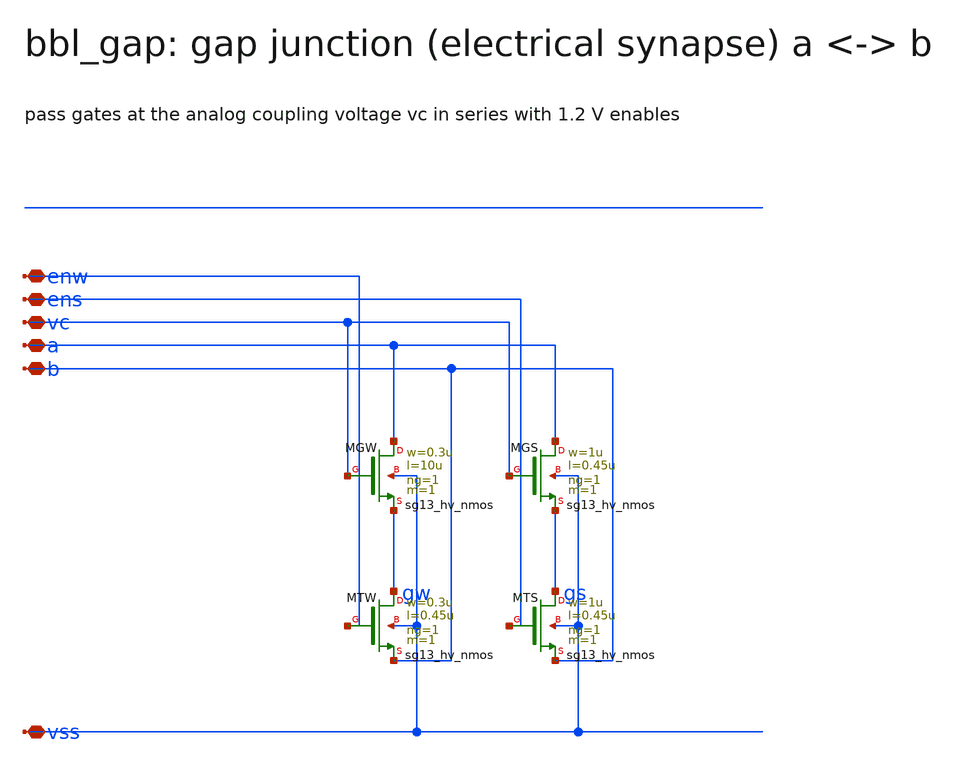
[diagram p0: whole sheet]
** sch_path: schematic/xschem/bbl_gap.sch
**.subckt bbl_gap vss a b vc enw ens
*.iopin vss
*.iopin a
*.iopin b
*.iopin vc
*.iopin enw
*.iopin ens
XMGW a vc gw vss sg13_hv_nmos w=0.3u l=10u ng=1 m=1 mm_ok=1
XMGS a vc gs vss sg13_hv_nmos w=1u l=0.45u ng=1 m=1 mm_ok=1
XMTW gw enw b vss sg13_hv_nmos w=0.3u l=0.45u ng=1 m=1 mm_ok=1
XMTS gs ens b vss sg13_hv_nmos w=1u l=0.45u ng=1 m=1 mm_ok=1
**.ends
.end
